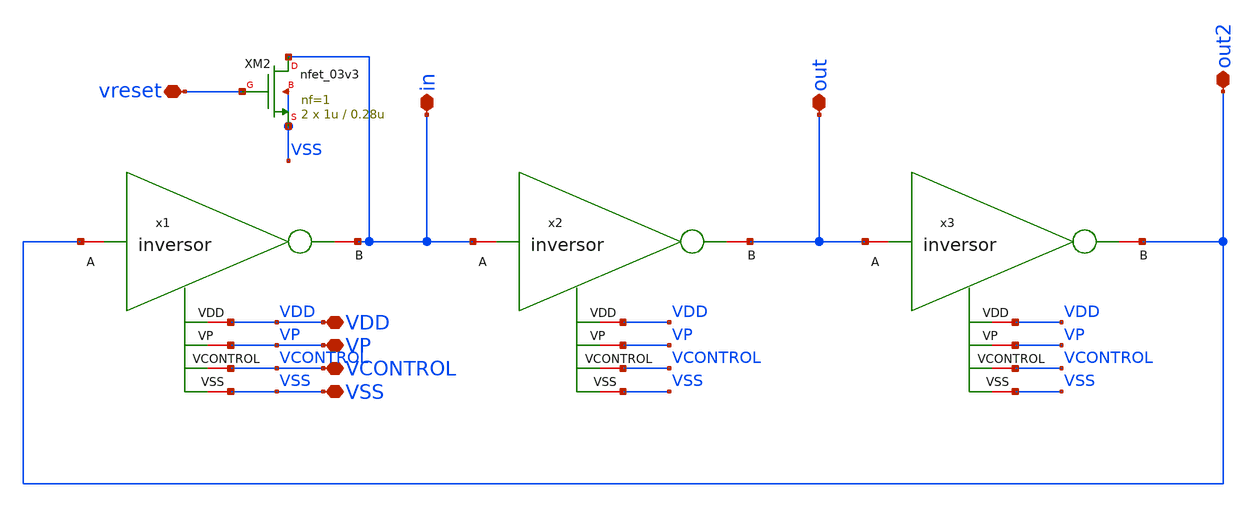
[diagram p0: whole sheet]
** sch_path: designs/ring_oscillator_pg/oscilador_completo.sch
**.subckt oscilador_completo in out out2 VDD VP VCONTROL VSS vreset
*.iopin in
*.iopin out
*.iopin out2
*.iopin VDD
*.iopin VP
*.iopin VCONTROL
*.iopin VSS
*.iopin vreset
XM2 in vreset VSS VSS nfet_03v3 L=0.28u W=1u nf=1 ad='int((nf+1)/2) * W/nf * 0.18u' as='int((nf+2)/2) * W/nf * 0.18u'
+ pd='2*int((nf+1)/2) * (W/nf + 0.18u)' ps='2*int((nf+2)/2) * (W/nf + 0.18u)' nrd='0.18u / W' nrs='0.18u / W'
+ sa=0 sb=0 sd=0 m=2
x1 VDD VP in out2 VCONTROL VSS inversor
x2 VDD VP out in VCONTROL VSS inversor
x3 VDD VP out2 out VCONTROL VSS inversor
**.ends

* expanding   symbol:  gf180/ring_oscillator_pg/inversor.sym # of pins=6
** sym_path: designs/ring_oscillator_pg/inversor.sym
** sch_path: designs/ring_oscillator_pg/inversor.sch
.subckt inversor VDD VP B A VCONTROL VSS
*.iopin B
*.iopin A
*.iopin VCONTROL
*.iopin VDD
*.iopin VP
*.iopin VSS
XM1 B A net1 VSS nfet_03v3 L=0.3u W={w} nf=1 ad='int((nf+1)/2) * W/nf * 0.18u' as='int((nf+2)/2) * W/nf * 0.18u'
+ pd='2*int((nf+1)/2) * (W/nf + 0.18u)' ps='2*int((nf+2)/2) * (W/nf + 0.18u)' nrd='0.18u / W' nrs='0.18u / W'
+ sa=0 sb=0 sd=0 m=1
XM2 B A net2 VDD pfet_03v3 L=0.3u W={wp} nf=1 ad='int((nf+1)/2) * W/nf * 0.18u' as='int((nf+2)/2) * W/nf * 0.18u'
+ pd='2*int((nf+1)/2) * (W/nf + 0.18u)' ps='2*int((nf+2)/2) * (W/nf + 0.18u)' nrd='0.18u / W' nrs='0.18u / W'
+ sa=0 sb=0 sd=0 m=1
XM3 net1 VCONTROL VSS VSS nfet_03v3 L=0.3u W={w} nf=1 ad='int((nf+1)/2) * W/nf * 0.18u' as='int((nf+2)/2) * W/nf * 0.18u'
+ pd='2*int((nf+1)/2) * (W/nf + 0.18u)' ps='2*int((nf+2)/2) * (W/nf + 0.18u)' nrd='0.18u / W' nrs='0.18u / W'
+ sa=0 sb=0 sd=0 m=2
XM4 net2 VP VDD VDD pfet_03v3 L=0.3u W={wp} nf=1 ad='int((nf+1)/2) * W/nf * 0.18u' as='int((nf+2)/2) * W/nf * 0.18u'
+ pd='2*int((nf+1)/2) * (W/nf + 0.18u)' ps='2*int((nf+2)/2) * (W/nf + 0.18u)' nrd='0.18u / W' nrs='0.18u / W'
+ sa=0 sb=0 sd=0 m=1
.ends

.end
